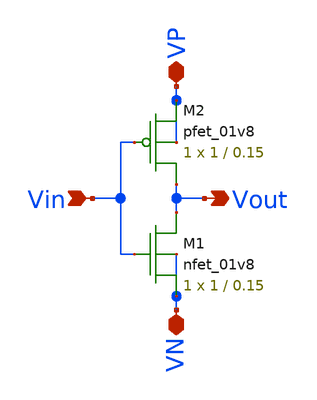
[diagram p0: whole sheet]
** sch_path: mini_proj_1/schematic/inverter.sch
**.subckt inverter Vin VP VN Vout
*.ipin Vin
*.iopin VP
*.iopin VN
*.opin Vout
XM1 Vout Vin VN VN sky130_fd_pr__nfet_01v8 L=0.15 W=1 nf=1 ad='int((nf+1)/2) * W/nf * 0.29' as='int((nf+2)/2) * W/nf * 0.29'
+ pd='2*int((nf+1)/2) * (W/nf + 0.29)' ps='2*int((nf+2)/2) * (W/nf + 0.29)' nrd='0.29 / W' nrs='0.29 / W'
+ sa=0 sb=0 sd=0 mult=1 m=1
XM2 Vout Vin VP VP sky130_fd_pr__pfet_01v8 L=0.15 W=1 nf=1 ad='int((nf+1)/2) * W/nf * 0.29' as='int((nf+2)/2) * W/nf * 0.29'
+ pd='2*int((nf+1)/2) * (W/nf + 0.29)' ps='2*int((nf+2)/2) * (W/nf + 0.29)' nrd='0.29 / W' nrs='0.29 / W'
+ sa=0 sb=0 sd=0 mult=1 m=1
**.ends
.end
